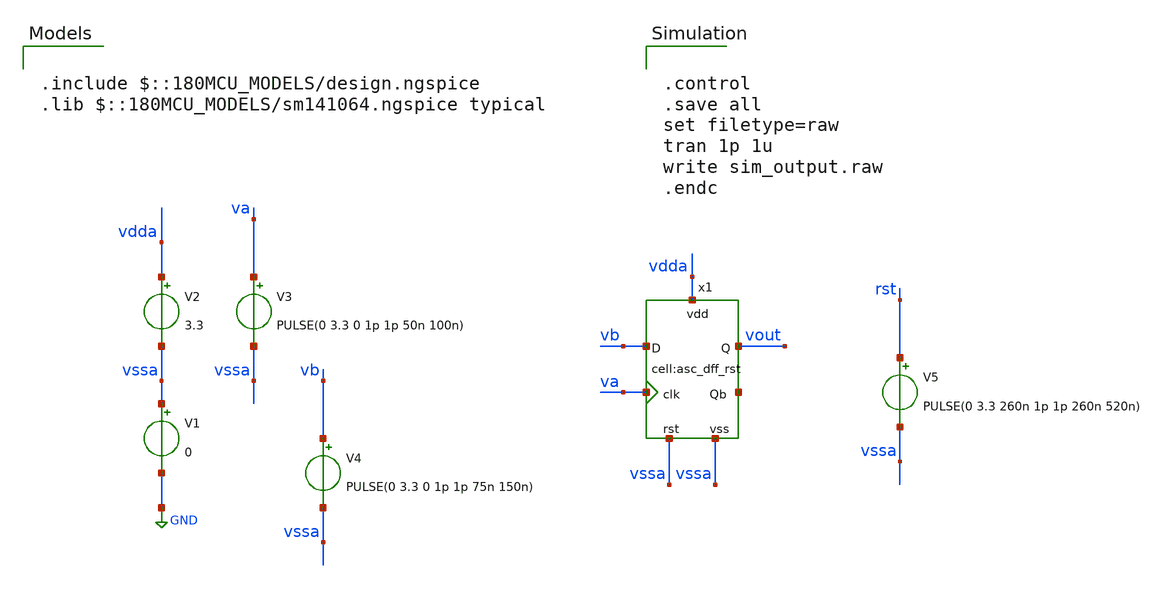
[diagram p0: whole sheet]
** sch_path: designs/libs/xp_tb_analog/tb_asc_dff_rst/tb_asc_dff_rst.sch
**.subckt tb_asc_dff_rst
V1 vssa GND 0
V2 vdda vssa 3.3
V3 va vssa PULSE(0 3.3 0 1p 1p 50n 100n)
V4 vb vssa PULSE(0 3.3 0 1p 1p 75n 150n)
x1 va vb net1 vdda vssa vout vssa asc_dff_rst
V5 rst vssa PULSE(0 3.3 260n 1p 1p 260n 520n)
**** begin user architecture code

.include $::180MCU_MODELS/design.ngspice
.lib $::180MCU_MODELS/sm141064.ngspice typical



.control
.save all
set filetype=raw
tran 1p 1u
write sim_output.raw
.endc


**** end user architecture code
**.ends
.GLOBAL GND
.end
